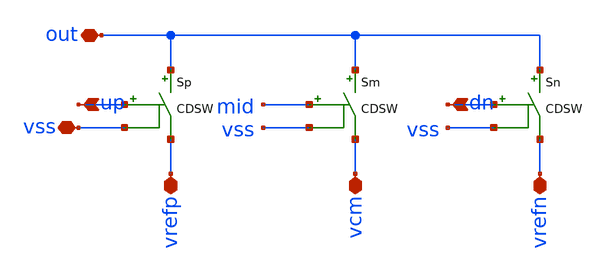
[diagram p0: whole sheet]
** sch_path: designs/libs/core_analog/saradc/mux3.sch
**.subckt mux3 out vrefp vcm vrefn up dn vss
*.iopin out
*.iopin vrefp
*.iopin vcm
*.iopin vrefn
*.ipin up
*.ipin dn
*.iopin vss
Sp out vrefp up vss CDSW
Sm out vcm mid vss CDSW
Sn out vrefn dn vss CDSW
**** begin user architecture code

Bmid mid vss V=((v(up,vss)<1.65)*(v(dn,vss)<1.65))*3.3


.model CDSW SW VT=0.9 VH=0.01 RON=0.01 ROFF=10G

**** end user architecture code
**.ends
.end
